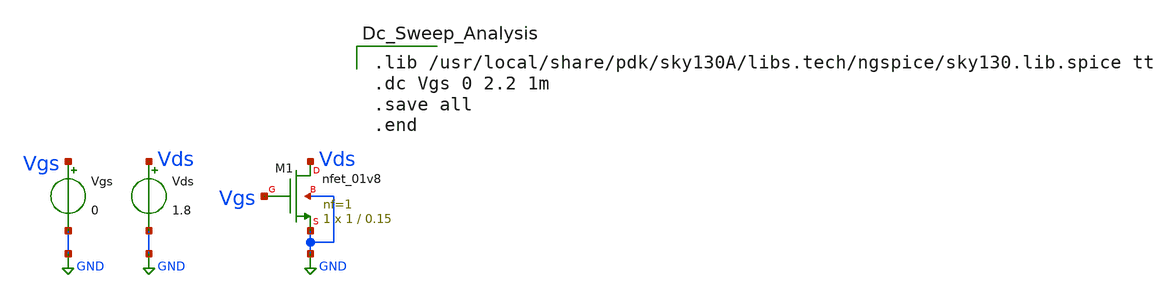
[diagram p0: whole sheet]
** sch_path: Schematics/nmos_analysis.sch
**.subckt nmos_analysis
Vgs Vgs GND 0
XM1 Vds Vgs GND GND sky130_fd_pr__nfet_01v8 L=0.15 W=1 nf=1 ad='int((nf+1)/2) * W/nf * 0.29' as='int((nf+2)/2) * W/nf * 0.29'
+ pd='2*int((nf+1)/2) * (W/nf + 0.29)' ps='2*int((nf+2)/2) * (W/nf + 0.29)' nrd='0.29 / W' nrs='0.29 / W'
+ sa=0 sb=0 sd=0 mult=1 m=1
Vds Vds GND 1.8
**** begin user architecture code

.lib /usr/local/share/pdk/sky130A/libs.tech/ngspice/sky130.lib.spice tt
.dc Vgs 0 2.2 1m
.save all
.end

**** end user architecture code
**.ends
.GLOBAL GND
.end
